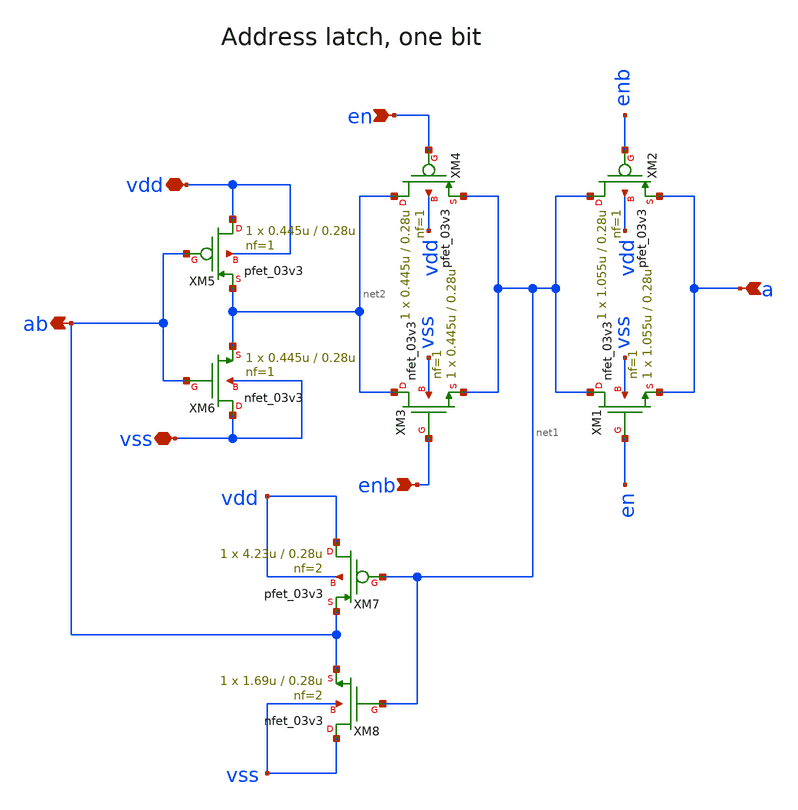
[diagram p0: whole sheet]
** sch_path: cells/gf180mcu_ocd_ip_sram__sram1024x8m8wm1/xschem/alatch_3v1024x8m81.sch
**.subckt alatch_3v1024x8m81 enb ab vdd vss en a
*.ipin enb
*.opin ab
*.iopin vdd
*.iopin vss
*.ipin en
*.ipin a
XM1 net1 en a vss nfet_03v3 L=0.28u W=1.055u nf=1 ad='int((nf+1)/2) * W/nf * 0.18u' as='int((nf+2)/2) * W/nf * 0.18u'
+ pd='2*int((nf+1)/2) * (W/nf + 0.18u)' ps='2*int((nf+2)/2) * (W/nf + 0.18u)' nrd='0.18u / W' nrs='0.18u / W'
+ sa=0 sb=0 sd=0 m=1
XM2 net1 enb a vdd pfet_03v3 L=0.28u W=1.055u nf=1 ad='int((nf+1)/2) * W/nf * 0.18u' as='int((nf+2)/2) * W/nf * 0.18u'
+ pd='2*int((nf+1)/2) * (W/nf + 0.18u)' ps='2*int((nf+2)/2) * (W/nf + 0.18u)' nrd='0.18u / W' nrs='0.18u / W'
+ sa=0 sb=0 sd=0 m=1
XM3 net2 enb net1 vss nfet_03v3 L=0.28u W=0.445u nf=1 ad='int((nf+1)/2) * W/nf * 0.18u' as='int((nf+2)/2) * W/nf * 0.18u'
+ pd='2*int((nf+1)/2) * (W/nf + 0.18u)' ps='2*int((nf+2)/2) * (W/nf + 0.18u)' nrd='0.18u / W' nrs='0.18u / W'
+ sa=0 sb=0 sd=0 m=1
XM4 net2 en net1 vdd pfet_03v3 L=0.28u W=0.445u nf=1 ad='int((nf+1)/2) * W/nf * 0.18u' as='int((nf+2)/2) * W/nf * 0.18u'
+ pd='2*int((nf+1)/2) * (W/nf + 0.18u)' ps='2*int((nf+2)/2) * (W/nf + 0.18u)' nrd='0.18u / W' nrs='0.18u / W'
+ sa=0 sb=0 sd=0 m=1
XM5 vdd ab net2 vdd pfet_03v3 L=0.28u W=0.445u nf=1 ad='int((nf+1)/2) * W/nf * 0.18u' as='int((nf+2)/2) * W/nf * 0.18u'
+ pd='2*int((nf+1)/2) * (W/nf + 0.18u)' ps='2*int((nf+2)/2) * (W/nf + 0.18u)' nrd='0.18u / W' nrs='0.18u / W'
+ sa=0 sb=0 sd=0 m=1
XM6 vss ab net2 vss nfet_03v3 L=0.28u W=0.445u nf=1 ad='int((nf+1)/2) * W/nf * 0.18u' as='int((nf+2)/2) * W/nf * 0.18u'
+ pd='2*int((nf+1)/2) * (W/nf + 0.18u)' ps='2*int((nf+2)/2) * (W/nf + 0.18u)' nrd='0.18u / W' nrs='0.18u / W'
+ sa=0 sb=0 sd=0 m=1
XM7 vdd net1 ab vdd pfet_03v3 L=0.28u W=4.23u nf=2 ad='int((nf+1)/2) * W/nf * 0.18u' as='int((nf+2)/2) * W/nf * 0.18u'
+ pd='2*int((nf+1)/2) * (W/nf + 0.18u)' ps='2*int((nf+2)/2) * (W/nf + 0.18u)' nrd='0.18u / W' nrs='0.18u / W'
+ sa=0 sb=0 sd=0 m=1
XM8 vss net1 ab vss nfet_03v3 L=0.28u W=1.69u nf=2 ad='int((nf+1)/2) * W/nf * 0.18u' as='int((nf+2)/2) * W/nf * 0.18u'
+ pd='2*int((nf+1)/2) * (W/nf + 0.18u)' ps='2*int((nf+2)/2) * (W/nf + 0.18u)' nrd='0.18u / W' nrs='0.18u / W'
+ sa=0 sb=0 sd=0 m=1
**.ends
.end
